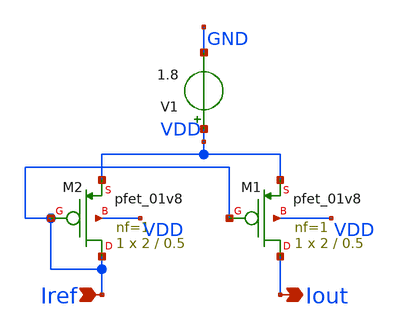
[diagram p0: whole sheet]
** sch_path: bias_mirror/bias_mirror.sch
**.subckt bias_mirror Iref Iout
*.ipin Iref
*.opin Iout
XM1 Iout Iref VDD VDD sky130_fd_pr__pfet_01v8 L=0.5 W=2 nf=1 ad='int((1 + 1)/2) * 2 / 1 * 0.29' as='int((1 + 2)/2) * 2 / 1 * 0.29'
+ pd='2*int((1 + 1)/2) * (2 / 1 + 0.29)' ps='2*int((1 + 2)/2) * (2 / 1 + 0.29)' nrd='0.29 / 2 ' nrs='0.29 / 2 '
+ sa=0 sb=0 sd=0 mult=1 m=1
XM2 Iref Iref VDD VDD sky130_fd_pr__pfet_01v8 L=0.5 W=2 nf=1 ad='int((1 + 1)/2) * 2 / 1 * 0.29' as='int((1 + 2)/2) * 2 / 1 * 0.29'
+ pd='2*int((1 + 1)/2) * (2 / 1 + 0.29)' ps='2*int((1 + 2)/2) * (2 / 1 + 0.29)' nrd='0.29 / 2 ' nrs='0.29 / 2 '
+ sa=0 sb=0 sd=0 mult=1 m=1
V1 VDD GND 1.8
**.ends
.end
